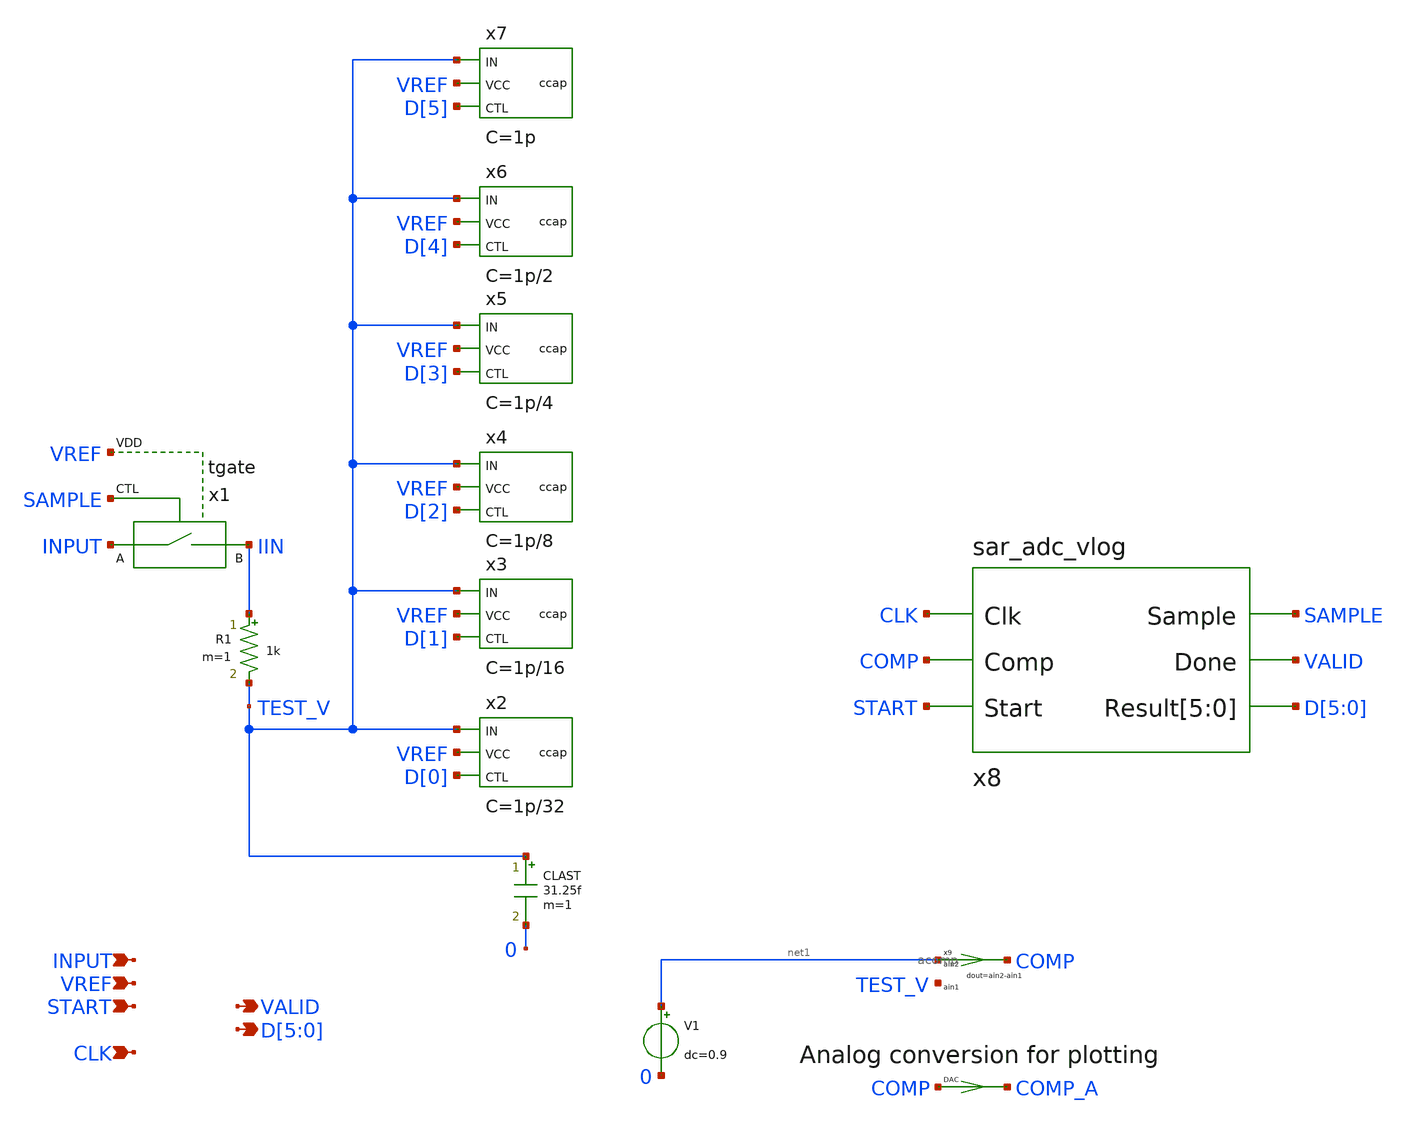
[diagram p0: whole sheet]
** sch_path: demo/cosim/vacask_cosim_hier/sar_adc.sch
**.subckt sar_adc INPUT VREF START VALID CLK D[5],D[4],D[3],D[2],D[1],D[0]
*.ipin INPUT
*.ipin VREF
*.ipin START
*.opin VALID
*.ipin CLK
*.opin D[5],D[4],D[3],D[2],D[1],D[0]
CLAST TEST_V 0 31.25f m=1
R1 IIN TEST_V 1k m=1
x1 INPUT IIN SAMPLE VREF tgate
x2 TEST_V VREF D[0] ccap C = 1p/32
x3 TEST_V VREF D[1] ccap C = 1p/16
x4 TEST_V VREF D[2] ccap C = 1p/8
x5 TEST_V VREF D[3] ccap C = 1p/4
x6 TEST_V VREF D[4] ccap C = 1p/2
x7 TEST_V VREF D[5] ccap C = 1p
x8 CLK COMP VALID D[5] D[4] D[3] D[2] D[1] D[0] SAMPLE START sar_adc_vlog
DAC COMP_A COMP dac_bridge
x9 COMP net1 TEST_V acomp
V1 net1 0 dc=0.9
**.ends
.end
